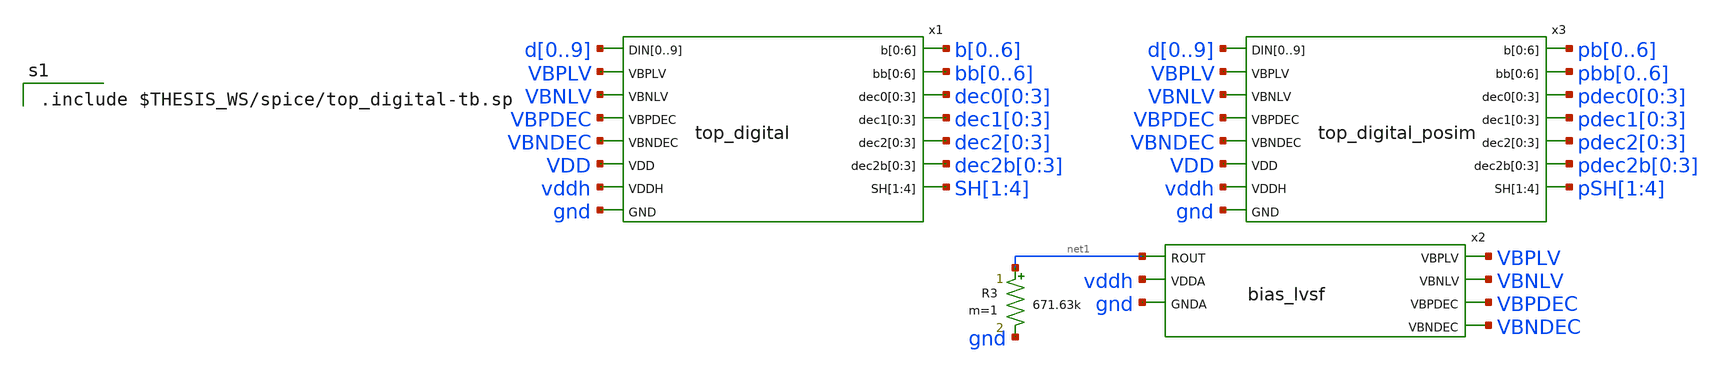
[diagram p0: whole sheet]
** sch_path: xschem/top_digital-tb.sch
.lib $::SKYWATER_MODELS/sky130.lib.spice tt
.include $::SKYWATER_STDCELLS/sky130_fd_sc_hd.spice
.include ~/pdk/sky130A/libs.ref/sky130_fd_sc_hvl/spice/sky130_fd_sc_hvl.spice

**.subckt top_digital-tb
x2 net1 VBPLV VBNLV VBPDEC VBNDEC vddh gnd bias_lvsf
R3 net1 gnd 671.63k m=1
x1 d0 d1 d2 d3 d4 d5 d6 d7 d8 d9 VBPLV VBNLV VBPDEC VBNDEC b0 b1 b2 b3 b4 b5 b6 bb0 bb1 bb2 bb3 bb4
+ bb5 bb6 dec0[0] dec0[1] dec0[2] dec0[3] dec1[0] dec1[1] dec1[2] dec1[3] dec2[0] dec2[1] dec2[2] dec2[3]
+ dec2b[0] dec2b[1] dec2b[2] dec2b[3] SH[1] SH[2] SH[3] SH[4] VDD vddh gnd top_digital
x3 d0 d1 d2 d3 d4 d5 d6 d7 d8 d9 VBPLV VBNLV VBPDEC VBNDEC pb0 pb1 pb2 pb3 pb4 pb5 pb6 pbb0 pbb1
+ pbb2 pbb3 pbb4 pbb5 pbb6 pdec0[0] pdec0[1] pdec0[2] pdec0[3] pdec1[0] pdec1[1] pdec1[2] pdec1[3]
+ pdec2[0] pdec2[1] pdec2[2] pdec2[3] pdec2b[0] pdec2b[1] pdec2b[2] pdec2b[3] pSH[1] pSH[2] pSH[3] pSH[4] VDD
+ vddh gnd top_digital_posim
**** begin user architecture code

.include $THESIS_WS/spice/top_digital-tb.sp

**** end user architecture code
**.ends
.end
